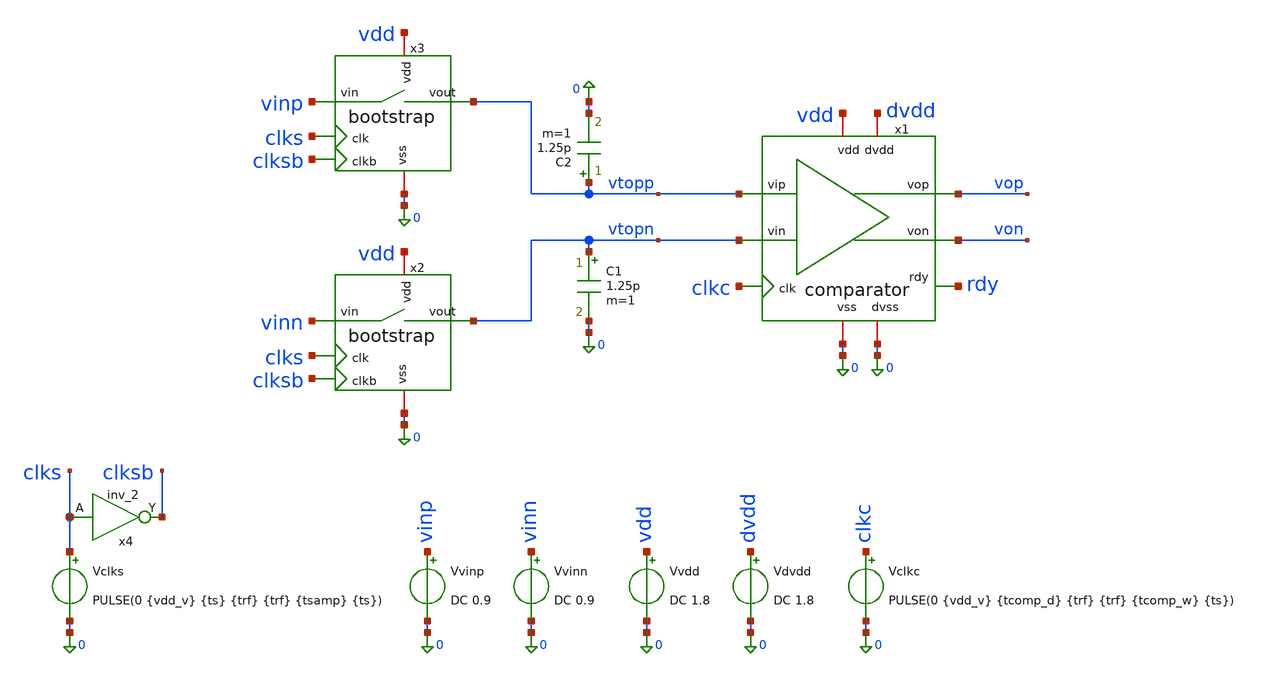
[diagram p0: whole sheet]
** sch_path: xschem/sar-adc_tb/tb4_kickback.sch
.lib $::SKYWATER_MODELS/sky130.lib.spice tt
.include $::SKYWATER_STDCELLS/sky130_fd_sc_hd.spice

**.subckt tb4_kickback
x1 vdd vop clkc von vtopp vtopn 0 dvdd 0 rdy comparator
x2 clks clksb vinn vtopn vdd 0 bootstrap
x3 clks clksb vinp vtopp vdd 0 bootstrap
C1 vtopn 0 1.25p m=1
C2 vtopp 0 1.25p m=1
Vclks clks 0 PULSE(0 {vdd_v} {ts} {trf} {trf} {tsamp} {ts})
x4 clks 0 0 dvdd dvdd clksb sky130_fd_sc_hd__inv_2
Vvinp vinp 0 DC 0.9
Vvinn vinn 0 DC 0.9
Vvdd vdd 0 DC 1.8
Vdvdd dvdd 0 DC 1.8
Vclkc clkc 0 PULSE(0 {vdd_v} {tcomp_d} {trf} {trf} {tcomp_w} {ts})
**** begin user architecture code


.param tcomp_d = 'ts + 20e-9'    $ strobe 5 ns setelah switch membuka
.param tcomp_w = 25e-9
.param vdd_v   = 1.8
.param fs      = 10e6
.param ts      = '1/fs'          $ 100 ns
.param tsamp   = 15e-9           $ jendela track
.param trf     = 100e-12         $ rise/fall clock (buffer riil, bukan 1 ps)




.control
  echo ''
  echo '=== TB4  kickback comparator ===================================='
  echo '1 LSB differential = 14.0625 mV.  Batas wajar: kickback'
  echo 'differential < 0.25 LSB = 3.5 mV, dan yang lebih penting,'
  echo 'VARIASI-nya terhadap kode input harus < 0.25 LSB (itu yang'
  echo 'jadi INL; bagian yang konstan hanya jadi offset).'
  echo ''

  foreach vd 0.00703 0.0703 0.703 1.700
    let vp = 0.9 + $vd/2
    let vn = 0.9 - $vd/2
    alter Vvinp dc = $&vp
    alter Vvinn dc = $&vn

    * ---- run A: comparator DIAM (referensi droop) -------------------
    alter @vclkc[pulse] = [ 0 0 120n 100p 100p 25n 100n ]
    tran 20p 400n
    setplot $curplot
    meas tran a0p FIND v(vtopp) AT=319.5n
    meas tran a0n FIND v(vtopn) AT=319.5n
    meas tran a1p FIND v(vtopp) AT=395n
    meas tran a1n FIND v(vtopn) AT=395n
    let ref_d  = (a1p - a1n) - (a0p - a0n)
    let ref_cm = (a1p + a1n)/2 - (a0p + a0n)/2
    * Tiap `tran` membuat PLOT BARU. Vektor dari run sebelumnya tidak
    * terlihat dari plot baru, jadi nilainya harus dipindah ke shell
    * variable dulu -- itu satu-satunya yang lintas-plot.
    set refd = $&ref_d
    set refcm = $&ref_cm

    * ---- run B: comparator MEN-STROBE -------------------------------
    alter @vclkc[pulse] = [ 0 1.8 120n 100p 100p 25n 100n ]
    tran 20p 400n
    setplot $curplot
    meas tran b0p FIND v(vtopp) AT=319.5n
    meas tran b0n FIND v(vtopn) AT=319.5n
    meas tran b1p FIND v(vtopp) AT=395n
    meas tran b1n FIND v(vtopn) AT=395n
    meas tran bpk MIN v(vtopp) FROM=320n TO=330n
    let act_d  = (b1p - b1n) - (b0p - b0n)
    let act_cm = (b1p + b1n)/2 - (b0p + b0n)/2

    * ---- kickback murni = selisih kedua run -------------------------
    let kb_d    = (act_d - $refd)*1e3
    let kb_cm   = (act_cm - $refcm)*1e3
    let kb_lsb  = kb_d/14.0625
    let kb_peak = (bpk - b0p)*1e3
    let vin_lsb = $vd/0.0140625
    meas tran vopf FIND v(vop) AT=140n

    echo '  vin_diff=$vd V ($&vin_lsb LSB) | kick_diff=$&kb_d mV ($&kb_lsb LSB) | kick_cm=$&kb_cm mV | peak_dip=$&kb_peak mV | vop=$&vopf V'
  end
  echo ''

  write tb4_kickback.raw v(vtopp) v(vtopn) v(clks) v(clkc) v(vop) v(von) v(rdy)
.endc


**** end user architecture code
**.ends

* expanding   symbol:  comparator.sym # of pins=10
** sym_path: xschem/sar-adc/comparator.sym
** sch_path: xschem/sar-adc/comparator.sch
.subckt comparator vdd vop clk von vip vin vss dvdd dvss rdy
*.ipin clk
*.ipin vip
*.ipin vin
*.iopin vdd
*.iopin vss
*.opin vop
*.opin von
*.iopin dvdd
*.iopin dvss
*.opin rdy
XMinputp pcp vip net1 vss sky130_fd_pr__nfet_01v8 L=0.2 W=5 nf=1 ad='int((1 + 1)/2) * 5 / 1 * 0.29' as='int((1 + 2)/2) * 5 / 1 * 0.29'
+ pd='2*int((1 + 1)/2) * (5 / 1 + 0.29)' ps='2*int((1 + 2)/2) * (5 / 1 + 0.29)' nrd='0.29 / 5 ' nrs='0.29 / 5 '
+ sa=0 sb=0 sd=0 mult=1 m=1
XMinputn pcn vin net1 vss sky130_fd_pr__nfet_01v8 L=0.2 W=5 nf=1 ad='int((1 + 1)/2) * 5 / 1 * 0.29' as='int((1 + 2)/2) * 5 / 1 * 0.29'
+ pd='2*int((1 + 1)/2) * (5 / 1 + 0.29)' ps='2*int((1 + 2)/2) * (5 / 1 + 0.29)' nrd='0.29 / 5 ' nrs='0.29 / 5 '
+ sa=0 sb=0 sd=0 mult=1 m=1
XM1a comp_von comp_vop pcp vss sky130_fd_pr__nfet_01v8 L=0.15 W=0.42 nf=1 ad='int((1 + 1)/2) * 0.42 / 1 * 0.29'
+ as='int((1 + 2)/2) * 0.42 / 1 * 0.29' pd='2*int((1 + 1)/2) * (0.42 / 1 + 0.29)' ps='2*int((1 + 2)/2) * (0.42 / 1 + 0.29)'
+ nrd='0.29 / 0.42 ' nrs='0.29 / 0.42 ' sa=0 sb=0 sd=0 mult=1 m=1
XM1b comp_vop comp_von pcn vss sky130_fd_pr__nfet_01v8 L=0.15 W=0.42 nf=1 ad='int((1 + 1)/2) * 0.42 / 1 * 0.29'
+ as='int((1 + 2)/2) * 0.42 / 1 * 0.29' pd='2*int((1 + 1)/2) * (0.42 / 1 + 0.29)' ps='2*int((1 + 2)/2) * (0.42 / 1 + 0.29)'
+ nrd='0.29 / 0.42 ' nrs='0.29 / 0.42 ' sa=0 sb=0 sd=0 mult=1 m=1
XM2a comp_von comp_vop vdd vdd sky130_fd_pr__pfet_01v8 L=0.15 W=0.42 nf=1 ad='int((1 + 1)/2) * 0.42 / 1 * 0.29'
+ as='int((1 + 2)/2) * 0.42 / 1 * 0.29' pd='2*int((1 + 1)/2) * (0.42 / 1 + 0.29)' ps='2*int((1 + 2)/2) * (0.42 / 1 + 0.29)'
+ nrd='0.29 / 0.42 ' nrs='0.29 / 0.42 ' sa=0 sb=0 sd=0 mult=1 m=1
XM2b comp_vop comp_von vdd vdd sky130_fd_pr__pfet_01v8 L=0.15 W=0.42 nf=1 ad='int((1 + 1)/2) * 0.42 / 1 * 0.29'
+ as='int((1 + 2)/2) * 0.42 / 1 * 0.29' pd='2*int((1 + 1)/2) * (0.42 / 1 + 0.29)' ps='2*int((1 + 2)/2) * (0.42 / 1 + 0.29)'
+ nrd='0.29 / 0.42 ' nrs='0.29 / 0.42 ' sa=0 sb=0 sd=0 mult=1 m=1
XMtail net1 clk vss vss sky130_fd_pr__nfet_01v8 L=0.15 W=0.42 nf=1 ad='int((1 + 1)/2) * 0.42 / 1 * 0.29'
+ as='int((1 + 2)/2) * 0.42 / 1 * 0.29' pd='2*int((1 + 1)/2) * (0.42 / 1 + 0.29)' ps='2*int((1 + 2)/2) * (0.42 / 1 + 0.29)'
+ nrd='0.29 / 0.42 ' nrs='0.29 / 0.42 ' sa=0 sb=0 sd=0 mult=1 m=1
XMS3 comp_vop clk vdd vdd sky130_fd_pr__pfet_01v8 L=0.15 W=0.42 nf=1 ad='int((1 + 1)/2) * 0.42 / 1 * 0.29'
+ as='int((1 + 2)/2) * 0.42 / 1 * 0.29' pd='2*int((1 + 1)/2) * (0.42 / 1 + 0.29)' ps='2*int((1 + 2)/2) * (0.42 / 1 + 0.29)'
+ nrd='0.29 / 0.42 ' nrs='0.29 / 0.42 ' sa=0 sb=0 sd=0 mult=1 m=1
XMS2 comp_von clk vdd vdd sky130_fd_pr__pfet_01v8 L=0.15 W=0.42 nf=1 ad='int((1 + 1)/2) * 0.42 / 1 * 0.29'
+ as='int((1 + 2)/2) * 0.42 / 1 * 0.29' pd='2*int((1 + 1)/2) * (0.42 / 1 + 0.29)' ps='2*int((1 + 2)/2) * (0.42 / 1 + 0.29)'
+ nrd='0.29 / 0.42 ' nrs='0.29 / 0.42 ' sa=0 sb=0 sd=0 mult=1 m=1
XMS4 pcn clk vdd vdd sky130_fd_pr__pfet_01v8 L=0.15 W=0.42 nf=1 ad='int((1 + 1)/2) * 0.42 / 1 * 0.29'
+ as='int((1 + 2)/2) * 0.42 / 1 * 0.29' pd='2*int((1 + 1)/2) * (0.42 / 1 + 0.29)' ps='2*int((1 + 2)/2) * (0.42 / 1 + 0.29)'
+ nrd='0.29 / 0.42 ' nrs='0.29 / 0.42 ' sa=0 sb=0 sd=0 mult=1 m=1
XMS1 pcp clk vdd vdd sky130_fd_pr__pfet_01v8 L=0.15 W=0.42 nf=1 ad='int((1 + 1)/2) * 0.42 / 1 * 0.29'
+ as='int((1 + 2)/2) * 0.42 / 1 * 0.29' pd='2*int((1 + 1)/2) * (0.42 / 1 + 0.29)' ps='2*int((1 + 2)/2) * (0.42 / 1 + 0.29)'
+ nrd='0.29 / 0.42 ' nrs='0.29 / 0.42 ' sa=0 sb=0 sd=0 mult=1 m=1
xnandp comp_vop net3 dvss dvss dvdd dvdd net2 sky130_fd_sc_hd__nand2_1
xnandn comp_von net2 dvss dvss dvdd dvdd net3 sky130_fd_sc_hd__nand2_1
xbuffp net2 dvss dvss dvdd dvdd von sky130_fd_sc_hd__buf_4
xbuffn net3 dvss dvss dvdd dvdd vop sky130_fd_sc_hd__buf_4
xnandrdy comp_von comp_vop dvss dvss dvdd dvdd net4 sky130_fd_sc_hd__nand2_1
xbuffrdy net4 dvss dvss dvdd dvdd rdy sky130_fd_sc_hd__buf_4
.ends


* expanding   symbol:  bootstrap.sym # of pins=6
** sym_path: xschem/sar-adc/bootstrap.sym
** sch_path: xschem/sar-adc/bootstrap.sch
.subckt bootstrap clk clkb vin vout vdd vss
*.ipin clk
*.ipin clkb
*.ipin vin
*.opin vout
*.iopin vdd
*.iopin vss
XMswitch vin vgate vout vss sky130_fd_pr__nfet_01v8 L=0.15 W=2 nf=1 ad='int((1 + 1)/2) * 2 / 1 * 0.29'
+ as='int((1 + 2)/2) * 2 / 1 * 0.29' pd='2*int((1 + 1)/2) * (2 / 1 + 0.29)' ps='2*int((1 + 2)/2) * (2 / 1 + 0.29)'
+ nrd='0.29 / 2 ' nrs='0.29 / 2 ' sa=0 sb=0 sd=0 mult=1 m=1
XMdisbot cbot vgate vin vss sky130_fd_pr__nfet_01v8 L=0.15 W=1 nf=1 ad='int((1 + 1)/2) * 1 / 1 * 0.29'
+ as='int((1 + 2)/2) * 1 / 1 * 0.29' pd='2*int((1 + 1)/2) * (1 / 1 + 0.29)' ps='2*int((1 + 2)/2) * (1 / 1 + 0.29)'
+ nrd='0.29 / 1 ' nrs='0.29 / 1 ' sa=0 sb=0 sd=0 mult=1 m=1
XCboot ctop cbot sky130_fd_pr__cap_mim_m3_1 W=10 L=10 MF=1 m=1
XMdistop vgate vgdistop ctop ctop sky130_fd_pr__pfet_01v8 L=0.15 W=1 nf=1 ad='int((1 + 1)/2) * 1 / 1 * 0.29'
+ as='int((1 + 2)/2) * 1 / 1 * 0.29' pd='2*int((1 + 1)/2) * (1 / 1 + 0.29)' ps='2*int((1 + 2)/2) * (1 / 1 + 0.29)'
+ nrd='0.29 / 1 ' nrs='0.29 / 1 ' sa=0 sb=0 sd=0 mult=1 m=1
XMchtop ctop vgate vdd ctop sky130_fd_pr__pfet_01v8 L=0.15 W=1 nf=1 ad='int((1 + 1)/2) * 1 / 1 * 0.29'
+ as='int((1 + 2)/2) * 1 / 1 * 0.29' pd='2*int((1 + 1)/2) * (1 / 1 + 0.29)' ps='2*int((1 + 2)/2) * (1 / 1 + 0.29)'
+ nrd='0.29 / 1 ' nrs='0.29 / 1 ' sa=0 sb=0 sd=0 mult=1 m=1
XMdistopdrv vgdistop vgate cbot vss sky130_fd_pr__nfet_01v8 L=0.15 W=0.5 nf=1 ad='int((1 + 1)/2) * 0.5 / 1 * 0.29'
+ as='int((1 + 2)/2) * 0.5 / 1 * 0.29' pd='2*int((1 + 1)/2) * (0.5 / 1 + 0.29)' ps='2*int((1 + 2)/2) * (0.5 / 1 + 0.29)'
+ nrd='0.29 / 0.5 ' nrs='0.29 / 0.5 ' sa=0 sb=0 sd=0 mult=1 m=1
XMchtopdrv2 vschtopdrv1 clkb vss vss sky130_fd_pr__nfet_01v8 L=0.15 W=1 nf=1 ad='int((1 + 1)/2) * 1 / 1 * 0.29'
+ as='int((1 + 2)/2) * 1 / 1 * 0.29' pd='2*int((1 + 1)/2) * (1 / 1 + 0.29)' ps='2*int((1 + 2)/2) * (1 / 1 + 0.29)'
+ nrd='0.29 / 1 ' nrs='0.29 / 1 ' sa=0 sb=0 sd=0 mult=1 m=1
XMchbot cbot clkb vss vss sky130_fd_pr__nfet_01v8 L=0.15 W=1 nf=1 ad='int((1 + 1)/2) * 1 / 1 * 0.29'
+ as='int((1 + 2)/2) * 1 / 1 * 0.29' pd='2*int((1 + 1)/2) * (1 / 1 + 0.29)' ps='2*int((1 + 2)/2) * (1 / 1 + 0.29)'
+ nrd='0.29 / 1 ' nrs='0.29 / 1 ' sa=0 sb=0 sd=0 mult=1 m=1
XM1 vgdistop clk vdd vdd sky130_fd_pr__pfet_01v8 L=0.15 W=1 nf=1 ad='int((1 + 1)/2) * 1 / 1 * 0.29' as='int((1 + 2)/2) * 1 / 1 * 0.29'
+ pd='2*int((1 + 1)/2) * (1 / 1 + 0.29)' ps='2*int((1 + 2)/2) * (1 / 1 + 0.29)' nrd='0.29 / 1 ' nrs='0.29 / 1 '
+ sa=0 sb=0 sd=0 mult=1 m=1
XM2 vgdistop clk cbot vss sky130_fd_pr__nfet_01v8 L=0.15 W=0.5 nf=1 ad='int((1 + 1)/2) * 0.5 / 1 * 0.29'
+ as='int((1 + 2)/2) * 0.5 / 1 * 0.29' pd='2*int((1 + 1)/2) * (0.5 / 1 + 0.29)' ps='2*int((1 + 2)/2) * (0.5 / 1 + 0.29)'
+ nrd='0.29 / 0.5 ' nrs='0.29 / 0.5 ' sa=0 sb=0 sd=0 mult=1 m=1
XXMchtopdrv1 vgate vdd vschtopdrv1 vss sky130_fd_pr__nfet_g5v0d10v5 L=0.5 W=3 nf=1 ad='int((1 + 1)/2) * 3 / 1 * 0.29'
+ as='int((1 + 2)/2) * 3 / 1 * 0.29' pd='2*int((1 + 1)/2) * (3 / 1 + 0.29)' ps='2*int((1 + 2)/2) * (3 / 1 + 0.29)'
+ nrd='0.29 / 3 ' nrs='0.29 / 3 ' sa=0 sb=0 sd=0 mult=1 m=1
.ends

.end
